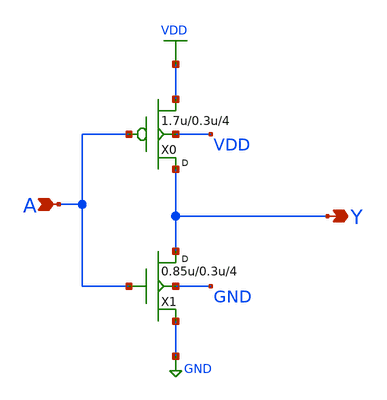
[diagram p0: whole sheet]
** sch_path: gf180mcu_osu_sc_gp12t3v3/cells/clkinv/gf180mcu_osu_sc_gp12t3v3__clkinv_4.sch
**.subckt gf180mcu_osu_sc_gp12t3v3__clkinv_4 A Y
*.ipin A
*.opin Y
X0 Y A VDD VDD pfet_03p3 w=1.7u l=0.3u m=4
X1 Y A GND GND nfet_03p3 w=0.85u l=0.3u m=4
**.ends
.GLOBAL VDD
.GLOBAL GND
.end
